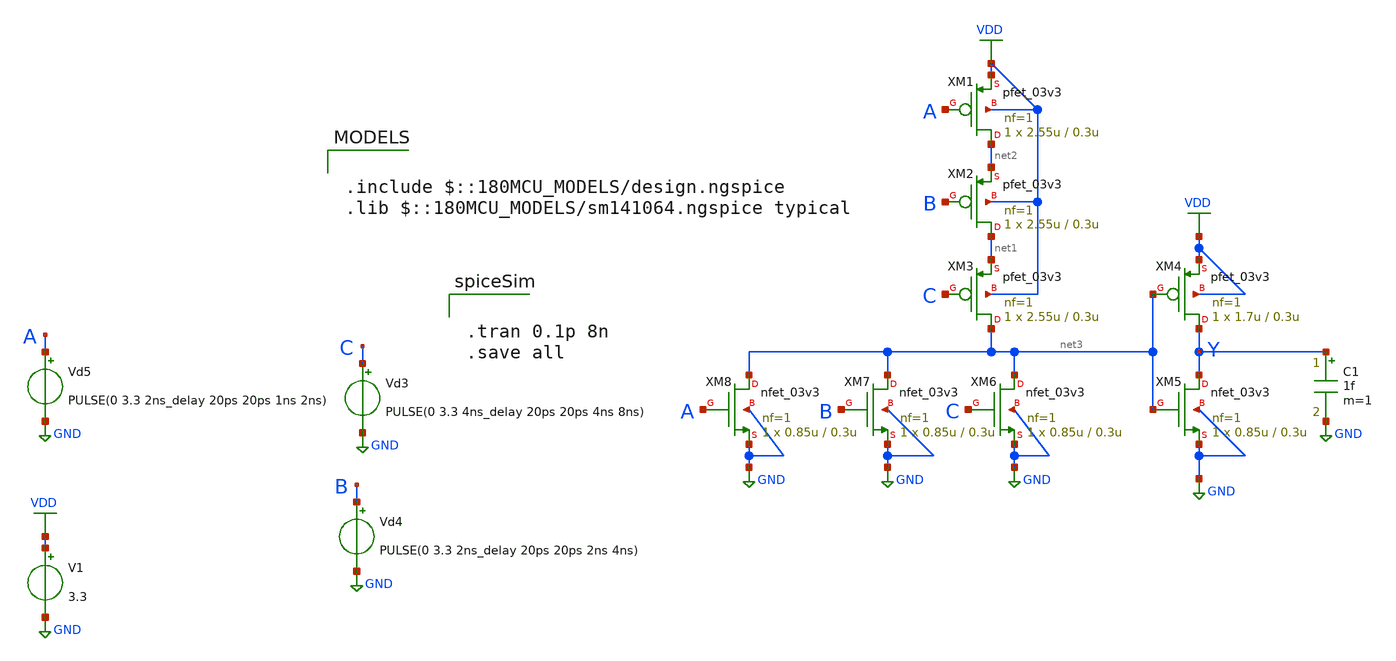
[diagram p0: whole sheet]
** sch_path: or3_1.sch
**.subckt or3_1
Vd3 C GND PULSE(0 3.3 4ns_delay 20ps 20ps 4ns 8ns)
Vd4 B GND PULSE(0 3.3 2ns_delay 20ps 20ps 2ns 4ns)
Vd5 A GND PULSE(0 3.3 2ns_delay 20ps 20ps 1ns 2ns)
V1 VDD GND 3.3
XM1 net2 A VDD VDD pfet_03v3 L=0.3u W=2.55u nf=1 ad='int((nf+1)/2) * W/nf * 0.18u' as='int((nf+2)/2) * W/nf * 0.18u'
+ pd='2*int((nf+1)/2) * (W/nf + 0.18u)' ps='2*int((nf+2)/2) * (W/nf + 0.18u)' nrd='0.18u / W' nrs='0.18u / W'
+ sa=0 sb=0 sd=0 m=1
XM2 net1 B net2 VDD pfet_03v3 L=0.3u W=2.55u nf=1 ad='int((nf+1)/2) * W/nf * 0.18u' as='int((nf+2)/2) * W/nf * 0.18u'
+ pd='2*int((nf+1)/2) * (W/nf + 0.18u)' ps='2*int((nf+2)/2) * (W/nf + 0.18u)' nrd='0.18u / W' nrs='0.18u / W'
+ sa=0 sb=0 sd=0 m=1
XM3 net3 C net1 VDD pfet_03v3 L=0.3u W=2.55u nf=1 ad='int((nf+1)/2) * W/nf * 0.18u' as='int((nf+2)/2) * W/nf * 0.18u'
+ pd='2*int((nf+1)/2) * (W/nf + 0.18u)' ps='2*int((nf+2)/2) * (W/nf + 0.18u)' nrd='0.18u / W' nrs='0.18u / W'
+ sa=0 sb=0 sd=0 m=1
XM4 Y net3 VDD VDD pfet_03v3 L=0.3u W=1.7u nf=1 ad='int((nf+1)/2) * W/nf * 0.18u' as='int((nf+2)/2) * W/nf * 0.18u'
+ pd='2*int((nf+1)/2) * (W/nf + 0.18u)' ps='2*int((nf+2)/2) * (W/nf + 0.18u)' nrd='0.18u / W' nrs='0.18u / W'
+ sa=0 sb=0 sd=0 m=1
XM5 Y net3 GND GND nfet_03v3 L=0.3u W=0.85u nf=1 ad='int((nf+1)/2) * W/nf * 0.18u' as='int((nf+2)/2) * W/nf * 0.18u'
+ pd='2*int((nf+1)/2) * (W/nf + 0.18u)' ps='2*int((nf+2)/2) * (W/nf + 0.18u)' nrd='0.18u / W' nrs='0.18u / W'
+ sa=0 sb=0 sd=0 m=1
XM6 net3 C GND GND nfet_03v3 L=0.3u W=0.85u nf=1 ad='int((nf+1)/2) * W/nf * 0.18u' as='int((nf+2)/2) * W/nf * 0.18u'
+ pd='2*int((nf+1)/2) * (W/nf + 0.18u)' ps='2*int((nf+2)/2) * (W/nf + 0.18u)' nrd='0.18u / W' nrs='0.18u / W'
+ sa=0 sb=0 sd=0 m=1
XM7 net3 B GND GND nfet_03v3 L=0.3u W=0.85u nf=1 ad='int((nf+1)/2) * W/nf * 0.18u' as='int((nf+2)/2) * W/nf * 0.18u'
+ pd='2*int((nf+1)/2) * (W/nf + 0.18u)' ps='2*int((nf+2)/2) * (W/nf + 0.18u)' nrd='0.18u / W' nrs='0.18u / W'
+ sa=0 sb=0 sd=0 m=1
XM8 net3 A GND GND nfet_03v3 L=0.3u W=0.85u nf=1 ad='int((nf+1)/2) * W/nf * 0.18u' as='int((nf+2)/2) * W/nf * 0.18u'
+ pd='2*int((nf+1)/2) * (W/nf + 0.18u)' ps='2*int((nf+2)/2) * (W/nf + 0.18u)' nrd='0.18u / W' nrs='0.18u / W'
+ sa=0 sb=0 sd=0 m=1
C1 Y GND 1f m=1
**** begin user architecture code

.include $::180MCU_MODELS/design.ngspice
.lib $::180MCU_MODELS/sm141064.ngspice typical



.tran 0.1p 8n
.save all


**** end user architecture code
**.ends
.GLOBAL GND
.GLOBAL VDD
.end
